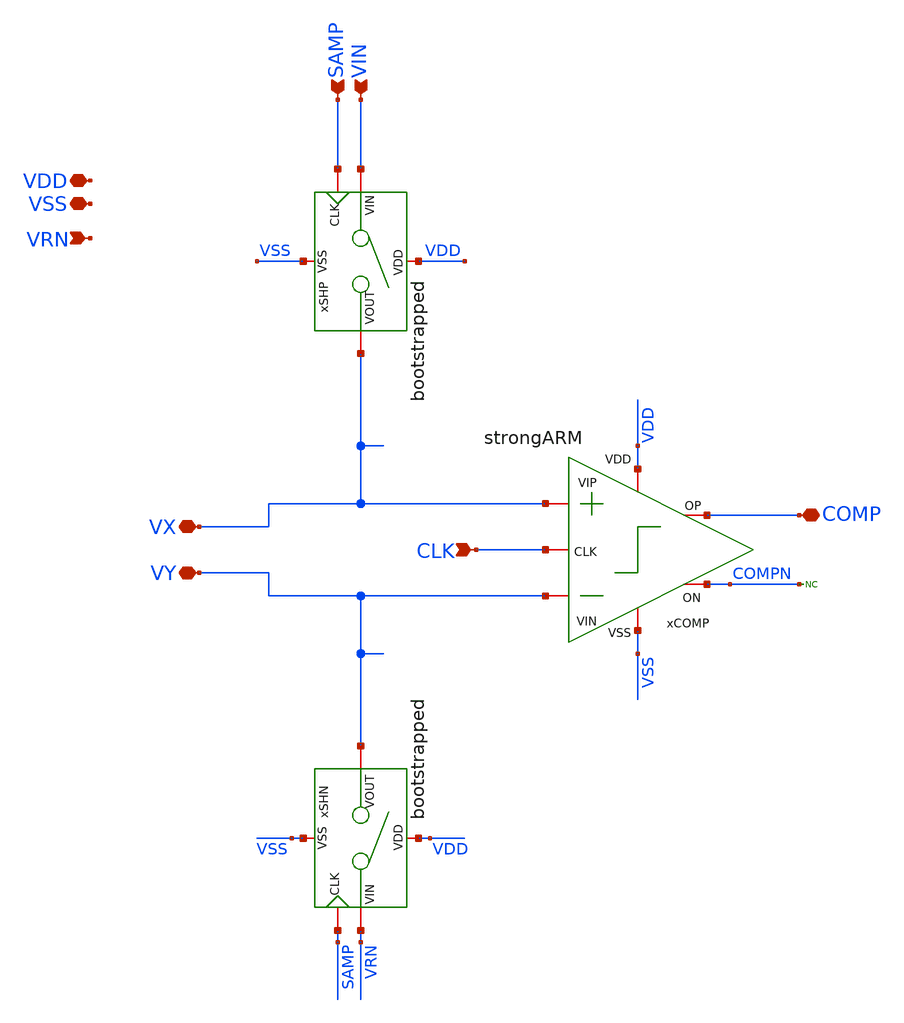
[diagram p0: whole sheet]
** sch_path: designs/sar_adc/top/VDAC/xschem/VDAC.sch
**.subckt VDAC VIN VY VX SAMP COMP CLK VSS VDD VRN
*.ipin VIN
*.iopin VY
*.iopin VX
*.ipin SAMP
*.iopin COMP
*.ipin CLK
*.iopin VSS
*.iopin VDD
*.ipin VRN
xSHP VDD VSS SAMP VIN VX bootstrapped
xSHN VDD VSS SAMP VRN VY bootstrapped
xCOMP VDD CLK COMPN COMP VY VX VSS strongARM
* noconn COMPN
**.ends
.end
